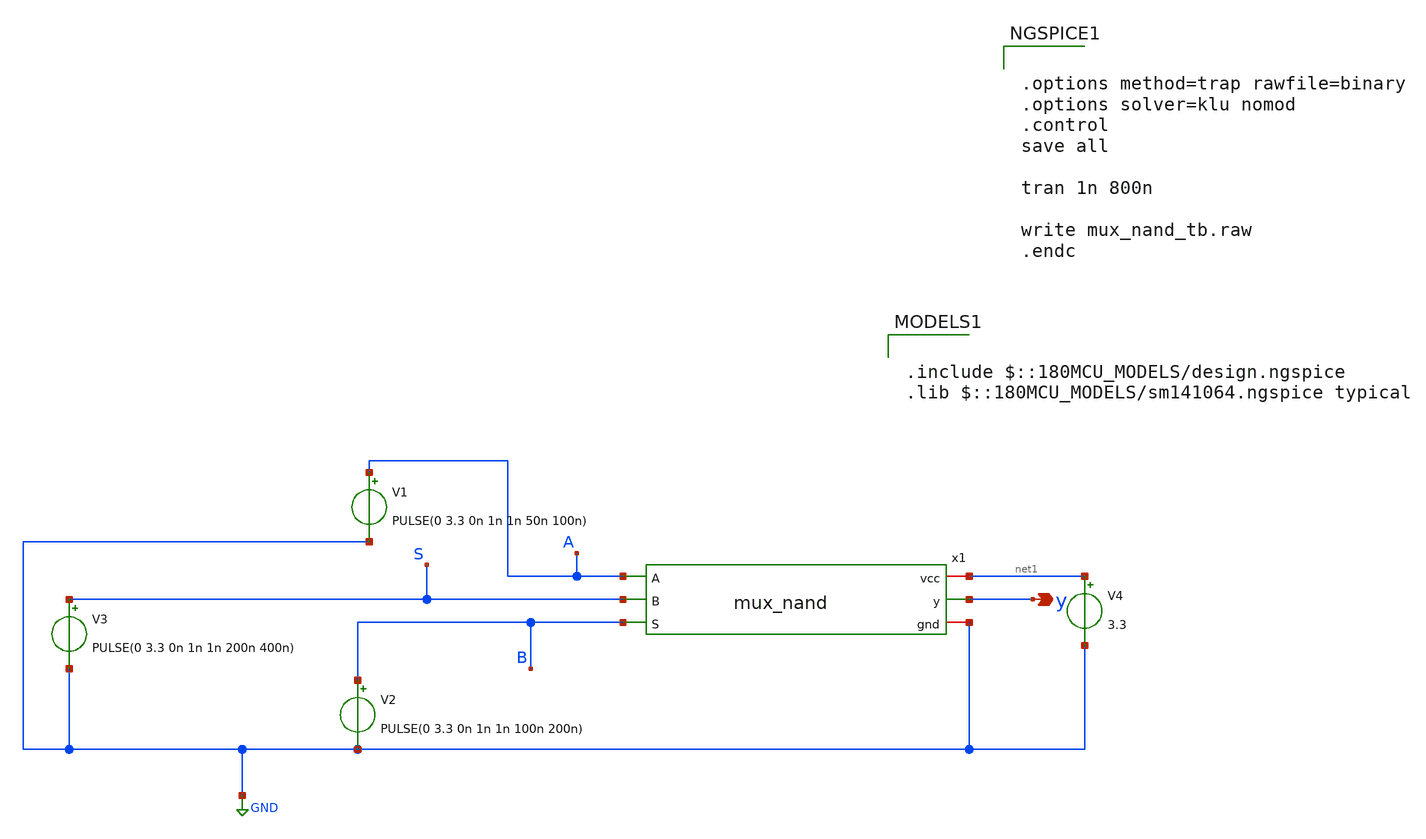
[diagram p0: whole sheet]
** sch_path: designs/schematics/mux2x1/mux_nand_tb.sch
**.subckt mux_nand_tb y
*.opin y
V1 A GND PULSE(0 3.3 0n 1n 1n 50n 100n)
V2 B GND PULSE(0 3.3 0n 1n 1n 100n 200n)
V3 S GND PULSE(0 3.3 0n 1n 1n 200n 400n)
V4 net1 GND 3.3
x1 net1 A y S B GND mux_nand
**** begin user architecture code


.options method=trap rawfile=binary
.options solver=klu nomod
.control
save all

tran 1n 800n

write mux_nand_tb.raw
.endc



.include $::180MCU_MODELS/design.ngspice
.lib $::180MCU_MODELS/sm141064.ngspice typical

**** end user architecture code
**.ends

* expanding   symbol:  voidwalkers-scandff-gf180mcu/designs/schematics/mux2x1/mux_nand.sym # of
*+ pins=6
** sym_path: designs/libs/mux2x1/mux_nand.sym
** sch_path: designs/libs/mux2x1/mux_nand.sch
.subckt mux_nand vcc A y B S gnd
*.ipin S
*.ipin A
*.ipin B
*.opin y
*.iopin vcc
*.iopin gnd
x1 vcc S net1 gnd inv
x2 vcc net2 A net1 gnd nand
x3 vcc net3 B S gnd nand
x4 vcc y net2 net3 gnd nand
.ends


* expanding   symbol:  voidwalkers-scandff-gf180mcu/designs/libs/mux2x1/inv.sym # of pins=4
** sym_path: designs/schematics/mux2x1/inv.sym
** sch_path: designs/schematics/mux2x1/inv.sch
.subckt inv vcc in out gnd
*.ipin in
*.opin out
*.iopin vcc
*.iopin gnd
XM2 out in vcc vcc pfet_03v3 L=0.28u W=0.22u nf=1 ad='int((nf+1)/2) * W/nf * 0.18u' as='int((nf+2)/2) * W/nf * 0.18u'
+ pd='2*int((nf+1)/2) * (W/nf + 0.18u)' ps='2*int((nf+2)/2) * (W/nf + 0.18u)' nrd='0.18u / W' nrs='0.18u / W'
+ sa=0 sb=0 sd=0 m=1
XM1 out in gnd gnd nfet_03v3 L=0.28u W=0.22u nf=1 ad='int((nf+1)/2) * W/nf * 0.18u' as='int((nf+2)/2) * W/nf * 0.18u'
+ pd='2*int((nf+1)/2) * (W/nf + 0.18u)' ps='2*int((nf+2)/2) * (W/nf + 0.18u)' nrd='0.18u / W' nrs='0.18u / W'
+ sa=0 sb=0 sd=0 m=1
.ends


* expanding   symbol:  voidwalkers-scandff-gf180mcu/designs/libs/mux2x1/nand.sym # of pins=5
** sym_path: designs/schematics/mux2x1/nand.sym
** sch_path: designs/schematics/mux2x1/nand.sch
.subckt nand vcc OUT A B gnd
*.ipin A
*.ipin B
*.opin OUT
*.iopin vcc
*.iopin gnd
XM1 OUT B net1 gnd nfet_03v3 L=0.28u W=0.22u nf=1 ad='int((nf+1)/2) * W/nf * 0.18u' as='int((nf+2)/2) * W/nf * 0.18u'
+ pd='2*int((nf+1)/2) * (W/nf + 0.18u)' ps='2*int((nf+2)/2) * (W/nf + 0.18u)' nrd='0.18u / W' nrs='0.18u / W'
+ sa=0 sb=0 sd=0 m=1
XM2 net1 A gnd gnd nfet_03v3 L=0.28u W=0.22u nf=1 ad='int((nf+1)/2) * W/nf * 0.18u' as='int((nf+2)/2) * W/nf * 0.18u'
+ pd='2*int((nf+1)/2) * (W/nf + 0.18u)' ps='2*int((nf+2)/2) * (W/nf + 0.18u)' nrd='0.18u / W' nrs='0.18u / W'
+ sa=0 sb=0 sd=0 m=1
XM3 OUT A vcc vcc pfet_03v3 L=0.28u W=0.22u nf=1 ad='int((nf+1)/2) * W/nf * 0.18u' as='int((nf+2)/2) * W/nf * 0.18u'
+ pd='2*int((nf+1)/2) * (W/nf + 0.18u)' ps='2*int((nf+2)/2) * (W/nf + 0.18u)' nrd='0.18u / W' nrs='0.18u / W'
+ sa=0 sb=0 sd=0 m=1
XM4 OUT B vcc vcc pfet_03v3 L=0.28u W=0.22u nf=1 ad='int((nf+1)/2) * W/nf * 0.18u' as='int((nf+2)/2) * W/nf * 0.18u'
+ pd='2*int((nf+1)/2) * (W/nf + 0.18u)' ps='2*int((nf+2)/2) * (W/nf + 0.18u)' nrd='0.18u / W' nrs='0.18u / W'
+ sa=0 sb=0 sd=0 m=1
.ends

.GLOBAL GND
.end
